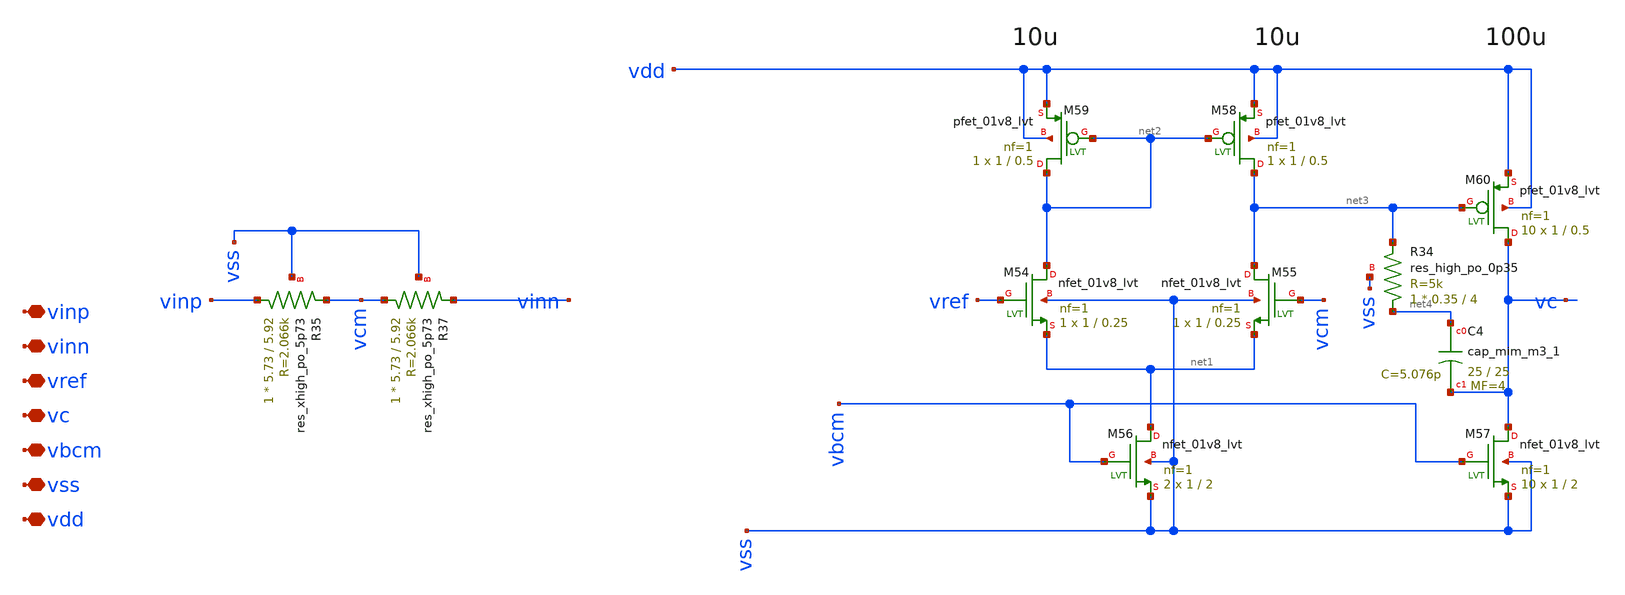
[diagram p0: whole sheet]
** sch_path: design/vga/cmfb1.sch
**.subckt cmfb1 vinp vinn vref vc vbcm vss vdd
*.iopin vinp
*.iopin vinn
*.iopin vref
*.iopin vc
*.iopin vbcm
*.iopin vss
*.iopin vdd
XM54 net2 vref net1 vss sky130_fd_pr__nfet_01v8_lvt L=0.25 W=1 nf=1 ad='int((nf+1)/2) * W/nf * 0.29'
+ as='int((nf+2)/2) * W/nf * 0.29' pd='2*int((nf+1)/2) * (W/nf + 0.29)' ps='2*int((nf+2)/2) * (W/nf + 0.29)'
+ nrd='0.29 / W' nrs='0.29 / W' sa=0 sb=0 sd=0 mult=1 m=1
XM55 net3 vcm net1 vss sky130_fd_pr__nfet_01v8_lvt L=0.25 W=1 nf=1 ad='int((nf+1)/2) * W/nf * 0.29' as='int((nf+2)/2) * W/nf * 0.29'
+ pd='2*int((nf+1)/2) * (W/nf + 0.29)' ps='2*int((nf+2)/2) * (W/nf + 0.29)' nrd='0.29 / W' nrs='0.29 / W'
+ sa=0 sb=0 sd=0 mult=1 m=1
XM56 net1 vbcm vss vss sky130_fd_pr__nfet_01v8_lvt L=2 W=1 nf=1 ad='int((nf+1)/2) * W/nf * 0.29' as='int((nf+2)/2) * W/nf * 0.29'
+ pd='2*int((nf+1)/2) * (W/nf + 0.29)' ps='2*int((nf+2)/2) * (W/nf + 0.29)' nrd='0.29 / W' nrs='0.29 / W'
+ sa=0 sb=0 sd=0 mult=2 m=2
XM57 vc vbcm vss vss sky130_fd_pr__nfet_01v8_lvt L=2 W=1 nf=1 ad='int((nf+1)/2) * W/nf * 0.29' as='int((nf+2)/2) * W/nf * 0.29'
+ pd='2*int((nf+1)/2) * (W/nf + 0.29)' ps='2*int((nf+2)/2) * (W/nf + 0.29)' nrd='0.29 / W' nrs='0.29 / W'
+ sa=0 sb=0 sd=0 mult=10 m=10
XM58 net3 net2 vdd vdd sky130_fd_pr__pfet_01v8_lvt L=0.5 W=1 nf=1 ad='int((nf+1)/2) * W/nf * 0.29' as='int((nf+2)/2) * W/nf * 0.29'
+ pd='2*int((nf+1)/2) * (W/nf + 0.29)' ps='2*int((nf+2)/2) * (W/nf + 0.29)' nrd='0.29 / W' nrs='0.29 / W'
+ sa=0 sb=0 sd=0 mult=1 m=1
XM59 net2 net2 vdd vdd sky130_fd_pr__pfet_01v8_lvt L=0.5 W=1 nf=1 ad='int((nf+1)/2) * W/nf * 0.29' as='int((nf+2)/2) * W/nf * 0.29'
+ pd='2*int((nf+1)/2) * (W/nf + 0.29)' ps='2*int((nf+2)/2) * (W/nf + 0.29)' nrd='0.29 / W' nrs='0.29 / W'
+ sa=0 sb=0 sd=0 mult=1 m=1
XM60 vc net3 vdd vdd sky130_fd_pr__pfet_01v8_lvt L=0.5 W=1 nf=1 ad='int((nf+1)/2) * W/nf * 0.29' as='int((nf+2)/2) * W/nf * 0.29'
+ pd='2*int((nf+1)/2) * (W/nf + 0.29)' ps='2*int((nf+2)/2) * (W/nf + 0.29)' nrd='0.29 / W' nrs='0.29 / W'
+ sa=0 sb=0 sd=0 mult=10 m=10
XR34 net4 net3 vss sky130_fd_pr__res_high_po_0p35 L=4 mult=1 m=1
XC4 net4 vc sky130_fd_pr__cap_mim_m3_1 W=25 L=25 MF=4 m=4
XR35 vinp vcm vss sky130_fd_pr__res_xhigh_po_5p73 L=5.92 mult=1 m=1
XR37 vcm vinn vss sky130_fd_pr__res_xhigh_po_5p73 L=5.92 mult=1 m=1
**.ends
.end
